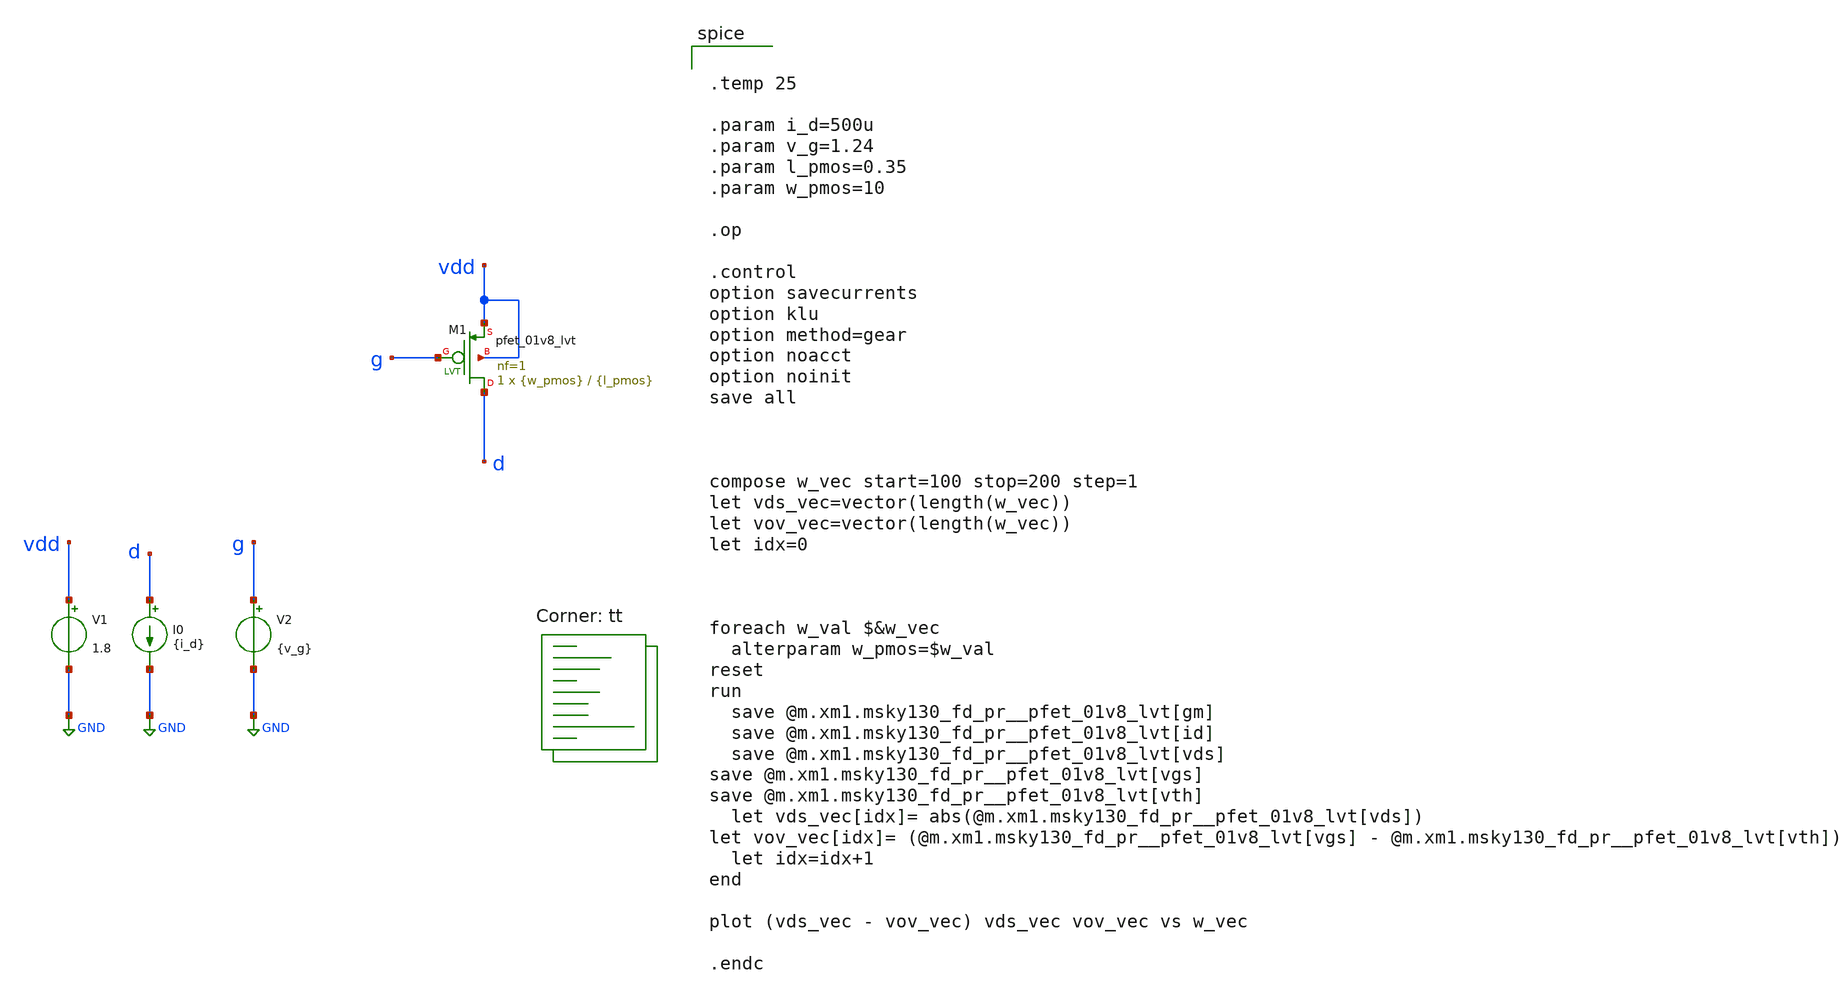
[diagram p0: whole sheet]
** sch_path: xschem/pmos_id_vgs.sch
**.subckt pmos_id_vgs
V1 vdd GND 1.8
.save i(v1)
I0 d GND {i_d}
V2 g GND {v_g}
.save i(v2)
XM1 d g vdd vdd sky130_fd_pr__pfet_01v8_lvt L={l_pmos} W={w_pmos} nf=1 ad='int((1 + 1)/2) * {w_pmos} / 1 * 0.29'
+ as='int((1 + 2)/2) * {w_pmos} / 1 * 0.29' pd='2*int((1 + 1)/2) * ({w_pmos} / 1 + 0.29)' ps='2*int((1 + 2)/2) * ({w_pmos} / 1 + 0.29)'
+ nrd='0.29 / {w_pmos} ' nrs='0.29 / {w_pmos} ' sa=0 sb=0 sd=0 mult=1 m=1
**** begin user architecture code
.lib $::SKYWATER_MODELS/sky130.lib.spice tt


.temp 25

.param i_d=500u
.param v_g=1.24
.param l_pmos=0.35
.param w_pmos=10

.op

.control
option savecurrents
option klu
option method=gear
option noacct
option noinit
save all



compose w_vec start=100 stop=200 step=1
let vds_vec=vector(length(w_vec))
let vov_vec=vector(length(w_vec))
let idx=0



foreach w_val $&w_vec
  alterparam w_pmos=$w_val
reset
run
  save @m.xm1.msky130_fd_pr__pfet_01v8_lvt[gm]
  save @m.xm1.msky130_fd_pr__pfet_01v8_lvt[id]
  save @m.xm1.msky130_fd_pr__pfet_01v8_lvt[vds]
save @m.xm1.msky130_fd_pr__pfet_01v8_lvt[vgs]
save @m.xm1.msky130_fd_pr__pfet_01v8_lvt[vth]
  let vds_vec[idx]= abs(@m.xm1.msky130_fd_pr__pfet_01v8_lvt[vds])
let vov_vec[idx]= (@m.xm1.msky130_fd_pr__pfet_01v8_lvt[vgs] -
+ @m.xm1.msky130_fd_pr__pfet_01v8_lvt[vth])
  let idx=idx+1
end

plot (vds_vec - vov_vec) vds_vec vov_vec vs w_vec

.endc

**** end user architecture code
**.ends
.GLOBAL GND
.end
